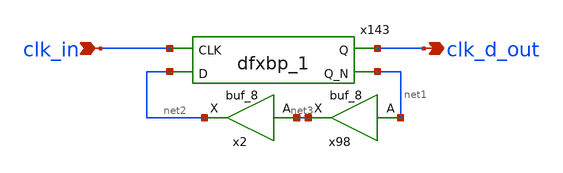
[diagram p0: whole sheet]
** sch_path: clk_divide.sch
**.subckt clk_divide clk_in clk_d_out
*.ipin clk_in
*.opin clk_d_out
x143 clk_in net2 GND GND VCC VCC clk_d_out net1 sky130_fd_sc_hd__dfxbp_1
x98 net1 GND GND VCC VCC net3 sky130_fd_sc_hd__buf_8
x2 net3 GND GND VCC VCC net2 sky130_fd_sc_hd__buf_8
**.ends
.end
